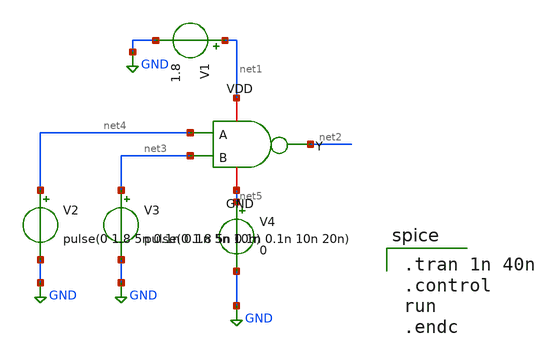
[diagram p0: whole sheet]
** sch_path: NAND_Test.sch
**.subckt NAND_Test
V1 net1 GND 1.8
V2 net4 GND pulse(0 1.8 5n 0.1n 0.1n 5n 10n)
V3 net3 GND pulse(0 1.8 5n 0.1n 0.1n 10n 20n)
V4 net5 GND 0
x1 net1 net2 net3 net4 net5 NAND
**** begin user architecture code
 .lib $::SKYWATER_MODELS/sky130.lib.spice tt

.tran 1n 40n
.control
run
.endc

**** end user architecture code
**.ends
.GLOBAL GND
.end
